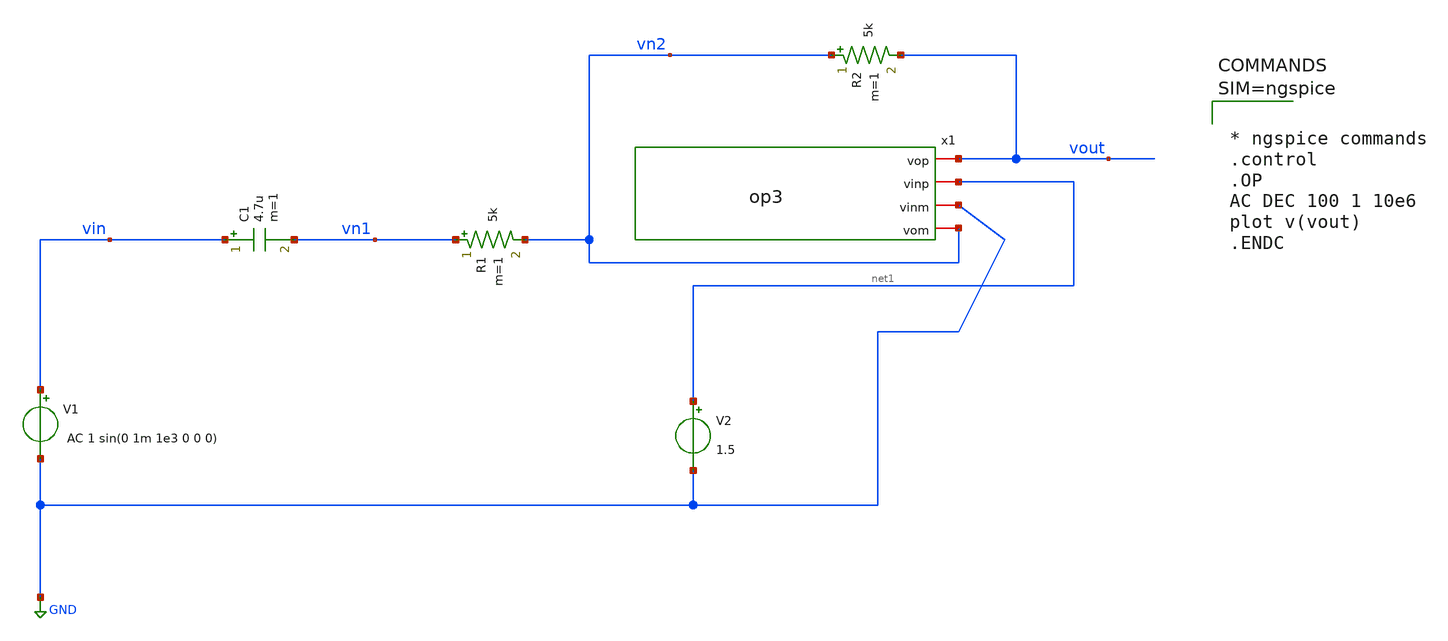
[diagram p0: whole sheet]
** sch_path: xschem/lp.sch
**.subckt lp
x1 vout net1 GND vn2 op3
R1 vn1 vn2 5k m=1
R2 vn2 vout 5k m=1
C1 vin vn1 4.7u m=1
V1 vin GND AC 1 sin(0 1m 1e3 0 0 0)
V2 net1 GND 1.5
**** begin user architecture code



* ngspice commands
.control
.OP
AC DEC 100 1 10e6
plot v(vout)
.ENDC




**** end user architecture code
**.ends

* expanding   symbol:  op3.sym # of pins=4
** sym_path: xschem/op3.sym
** sch_path: xschem/op3.sch
.subckt op3 vop vinp vinm vom
*.iopin vinp
*.iopin vinm
*.iopin vop
*.iopin vom
E1 net1 net3 vinp vinm 1000
E2 vop vom net2 net3 1000
R1 net1 net2 1k m=1
C1 net2 net3 160n m=1
.ends

.GLOBAL GND
.end
